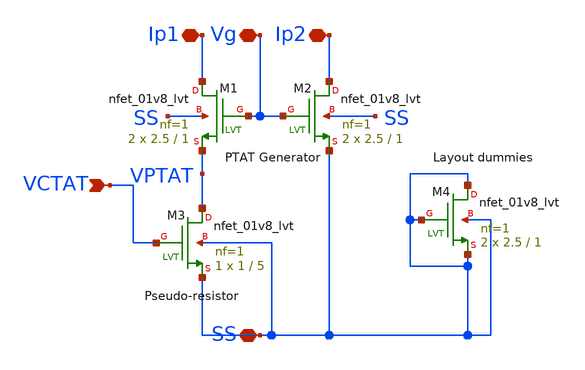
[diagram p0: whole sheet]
** sch_path: xschem/iref_2nA_igenerator.sch
**.subckt iref_2nA_igenerator SS VCTAT Ip1 Vg Ip2
*.iopin SS
*.ipin VCTAT
*.iopin Ip1
*.iopin Vg
*.iopin Ip2
XM1 Ip1 Vg VPTAT SS sky130_fd_pr__nfet_01v8_lvt L=1 W=2.5 nf=1 ad='int((nf+1)/2) * W/nf * 0.29' as='int((nf+2)/2) * W/nf * 0.29'
+ pd='2*int((nf+1)/2) * (W/nf + 0.29)' ps='2*int((nf+2)/2) * (W/nf + 0.29)' nrd='0.29 / W' nrs='0.29 / W'
+ sa=0 sb=0 sd=0 mult=2 m=2
XM2 Ip2 Vg SS SS sky130_fd_pr__nfet_01v8_lvt L=1 W=2.5 nf=1 ad='int((nf+1)/2) * W/nf * 0.29' as='int((nf+2)/2) * W/nf * 0.29'
+ pd='2*int((nf+1)/2) * (W/nf + 0.29)' ps='2*int((nf+2)/2) * (W/nf + 0.29)' nrd='0.29 / W' nrs='0.29 / W'
+ sa=0 sb=0 sd=0 mult=2 m=2
XM3 VPTAT VCTAT SS SS sky130_fd_pr__nfet_01v8_lvt L=5 W=1 nf=1 ad='int((nf+1)/2) * W/nf * 0.29' as='int((nf+2)/2) * W/nf * 0.29'
+ pd='2*int((nf+1)/2) * (W/nf + 0.29)' ps='2*int((nf+2)/2) * (W/nf + 0.29)' nrd='0.29 / W' nrs='0.29 / W'
+ sa=0 sb=0 sd=0 mult=1 m=1
XM4 SS SS SS SS sky130_fd_pr__nfet_01v8_lvt L=1 W=2.5 nf=1 ad='int((nf+1)/2) * W/nf * 0.29' as='int((nf+2)/2) * W/nf * 0.29'
+ pd='2*int((nf+1)/2) * (W/nf + 0.29)' ps='2*int((nf+2)/2) * (W/nf + 0.29)' nrd='0.29 / W' nrs='0.29 / W'
+ sa=0 sb=0 sd=0 mult=2 m=2
**.ends
.end
